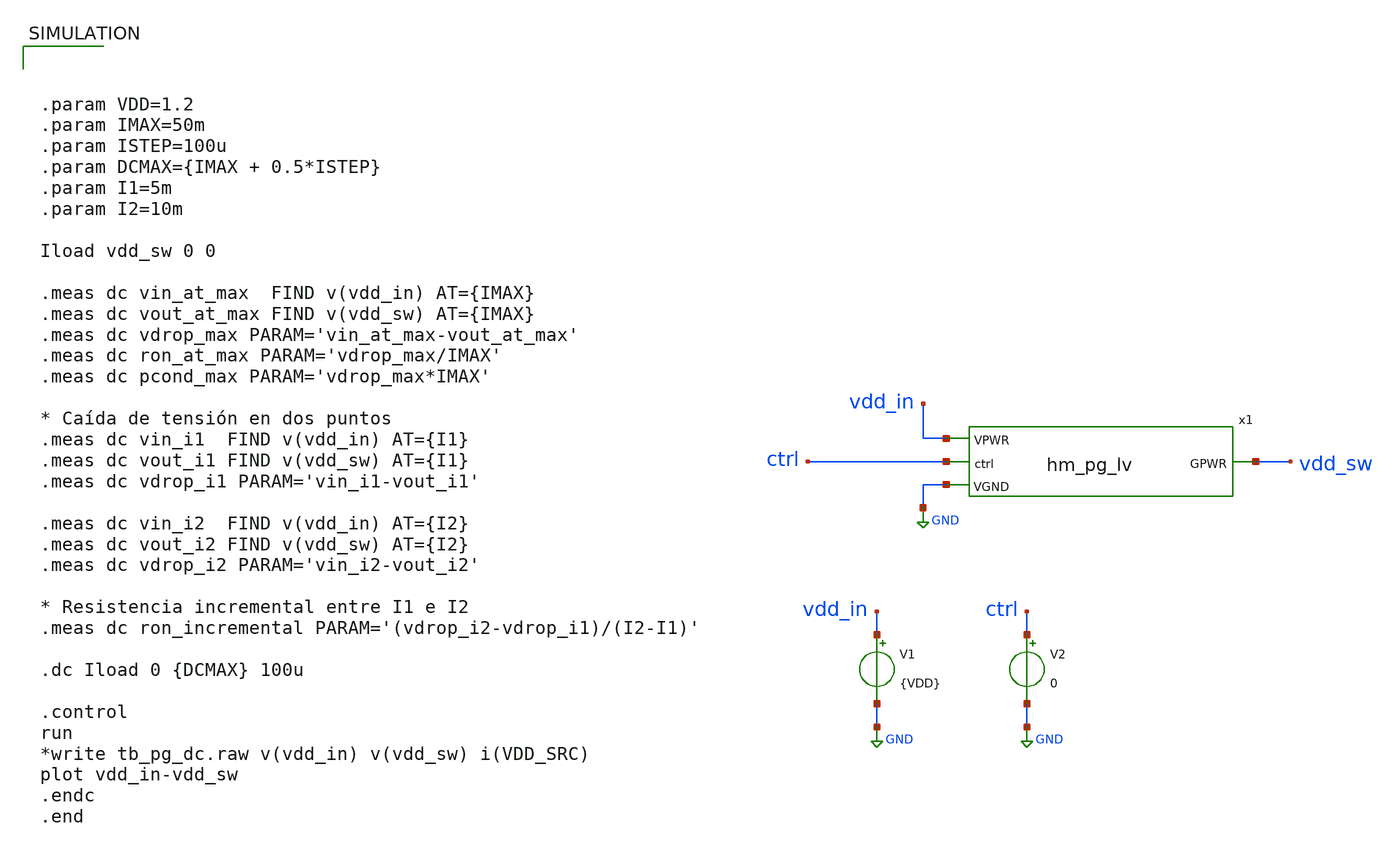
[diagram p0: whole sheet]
** sch_path: ihp-sg13cmos5l/libs.tech/xschem/tests/tb_hm_pg_lv_leakage.sch
**.subckt tb_hm_pg_lv_leakage
x1 vdd_in vdd_sw ctrl GND hm_pg_lv
V1 vdd_in GND {VDD}
V2 ctrl GND 0
**** begin user architecture code

.lib cornerMOSlv.lib mos_tt
*.lib cornerCAP.lib cap_typ




.param VDD=1.2
.param IMAX=50m
.param ISTEP=100u
.param DCMAX={IMAX + 0.5*ISTEP}
.param I1=5m
.param I2=10m

Iload vdd_sw 0 0

.meas dc vin_at_max  FIND v(vdd_in) AT={IMAX}
.meas dc vout_at_max FIND v(vdd_sw) AT={IMAX}
.meas dc vdrop_max PARAM='vin_at_max-vout_at_max'
.meas dc ron_at_max PARAM='vdrop_max/IMAX'
.meas dc pcond_max PARAM='vdrop_max*IMAX'

* Caída de tensión en dos puntos
.meas dc vin_i1  FIND v(vdd_in) AT={I1}
.meas dc vout_i1 FIND v(vdd_sw) AT={I1}
.meas dc vdrop_i1 PARAM='vin_i1-vout_i1'

.meas dc vin_i2  FIND v(vdd_in) AT={I2}
.meas dc vout_i2 FIND v(vdd_sw) AT={I2}
.meas dc vdrop_i2 PARAM='vin_i2-vout_i2'

* Resistencia incremental entre I1 e I2
.meas dc ron_incremental PARAM='(vdrop_i2-vdrop_i1)/(I2-I1)'

.dc Iload 0 {DCMAX} 100u

.control
run
*write tb_pg_dc.raw v(vdd_in) v(vdd_sw) i(VDD_SRC)
plot vdd_in-vdd_sw
.endc
.end


**** end user architecture code
**.ends

* expanding   symbol:  hm_analog/hm_pg_lv.sym # of pins=4
** sym_path: ihp-sg13cmos5l/libs.tech/xschem/hm_analog/hm_pg_lv.sym
** sch_path: ihp-sg13cmos5l/libs.tech/xschem/hm_analog/hm_pg_lv.sch
.subckt hm_pg_lv VPWR GPWR ctrl VGND
*.ipin ctrl
*.iopin VPWR
*.iopin VGND
*.iopin GPWR
XM1 ctrl_n ctrl VGND VGND sg13_lv_nmos w=2.6u l=0.13u ng=1 m=1 mm_ok=1
XM2 ctrl_n ctrl VPWR VPWR sg13_lv_pmos w=4.44u l=0.13u ng=1 m=1 mm_ok=1
XM3 GPWR ctrl_n VPWR VPWR sg13_lv_pmos w=2618u l=0.13u ng=374 m=2 mm_ok=1
x1 VGND GPWR ctrl_n dischg
.ends


* expanding   symbol:  hm_analog/dischg.sym # of pins=3
** sym_path: ihp-sg13cmos5l/libs.tech/xschem/hm_analog/dischg.sym
** sch_path: ihp-sg13cmos5l/libs.tech/xschem/hm_analog/dischg.sch
.subckt dischg VGND GPWR gate
*.iopin GPWR
*.iopin VGND
*.ipin gate
XM1 GPWR gate net2 VGND sg13_lv_nmos w=4u l=0.65u ng=1 m=1 mm_ok=1
XM2 net2 gate net3 VGND sg13_lv_nmos w=4u l=0.65u ng=1 m=1 mm_ok=1
XM3 net3 gate net4 VGND sg13_lv_nmos w=4u l=0.65u ng=1 m=1 mm_ok=1
XM4 net4 gate net1 VGND sg13_lv_nmos w=4u l=0.65u ng=1 m=1 mm_ok=1
XM5 net1 gate net7 VGND sg13_lv_nmos w=4u l=0.65u ng=1 m=1 mm_ok=1
XM6 net7 gate net6 VGND sg13_lv_nmos w=4u l=0.65u ng=1 m=1 mm_ok=1
XM7 net6 gate net5 VGND sg13_lv_nmos w=4u l=0.65u ng=1 m=1 mm_ok=1
XM8 net5 gate VGND VGND sg13_lv_nmos w=4u l=0.65u ng=1 m=1 mm_ok=1
XM9 GPWR gate net9 VGND sg13_lv_nmos w=4u l=0.65u ng=1 m=1 mm_ok=1
XM10 net9 gate net10 VGND sg13_lv_nmos w=4u l=0.65u ng=1 m=1 mm_ok=1
XM11 net10 gate net11 VGND sg13_lv_nmos w=4u l=0.65u ng=1 m=1 mm_ok=1
XM12 net11 gate net8 VGND sg13_lv_nmos w=4u l=0.65u ng=1 m=1 mm_ok=1
XM13 net8 gate net14 VGND sg13_lv_nmos w=4u l=0.65u ng=1 m=1 mm_ok=1
XM14 net14 gate net13 VGND sg13_lv_nmos w=4u l=0.65u ng=1 m=1 mm_ok=1
XM15 net13 gate net12 VGND sg13_lv_nmos w=4u l=0.65u ng=1 m=1 mm_ok=1
XM16 net12 gate VGND VGND sg13_lv_nmos w=4u l=0.65u ng=1 m=1 mm_ok=1
.ends

.GLOBAL GND
.end
